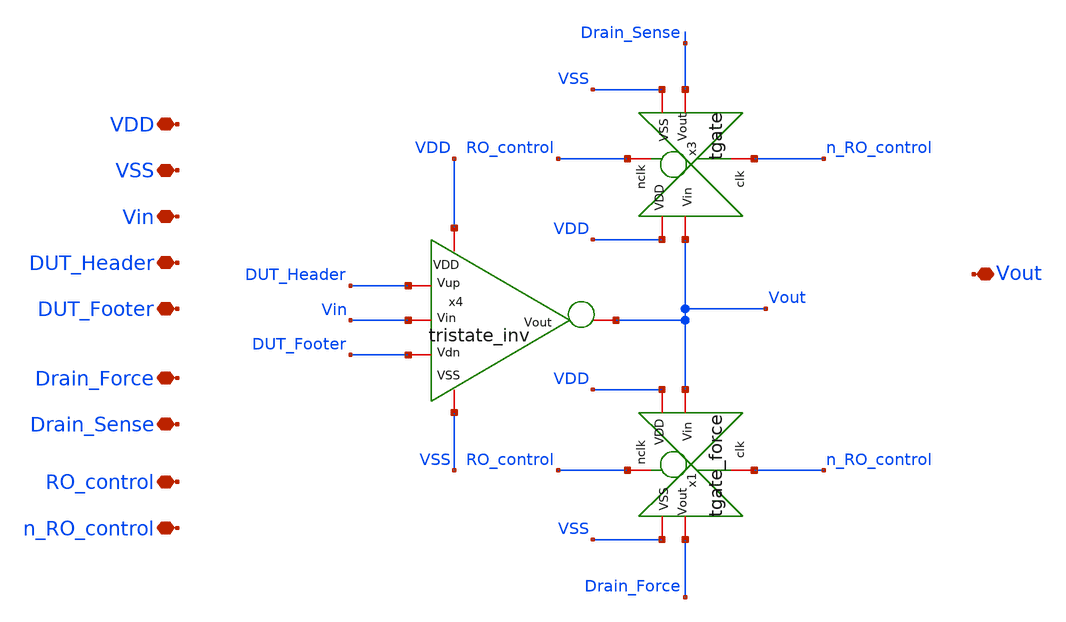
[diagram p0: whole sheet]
** sch_path: unic_cass_wrapper_user_project/ROs_reliability/rovcel1.sch
**.subckt rovcel1 VDD VSS Vin DUT_Header DUT_Footer Drain_Force Vout Drain_Sense RO_control
*+ n_RO_control
*.iopin VDD
*.iopin VSS
*.iopin Vin
*.iopin DUT_Header
*.iopin DUT_Footer
*.iopin Drain_Force
*.iopin Vout
*.iopin Drain_Sense
*.iopin RO_control
*.iopin n_RO_control
x4 VDD VSS Vin DUT_Header DUT_Footer Vout tristate_inv
x1 RO_control VDD Vout Drain_Force VSS n_RO_control tgate_force
x3 RO_control VDD Vout Drain_Sense VSS n_RO_control tgate
**.ends

* expanding   symbol:  tristate_inv.sym # of pins=6
** sym_path: tristate_inv.sym
** sch_path: tristate_inv.sch
.subckt tristate_inv VDD VSS Vin Vup Vdn Vout
*.iopin VDD
*.iopin VSS
*.iopin Vin
*.iopin Vout
*.iopin Vup
*.iopin Vdn
XM5 Vout Vin net1 VDD sg13_lv_pmos w=3.4u l=0.45u ng=1 m=4 mm_ok=1
XM2 net2 Vin Vout VSS sg13_lv_nmos w=1.3u l=0.45u ng=1 m=4 mm_ok=1
XM1 net1 Vup VDD VDD sg13_lv_pmos w=3.4u l=0.45u ng=1 m=12 mm_ok=1
XM3 VSS Vdn net2 VSS sg13_lv_nmos w=1.3u l=0.45u ng=1 m=12 mm_ok=1
.ends


* expanding   symbol:  tgate_force.sym # of pins=6
** sym_path: tgate_force.sym
** sch_path: tgate_force.sch
.subckt tgate_force nclk VDD Vin Vout VSS clk
*.iopin nclk
*.iopin clk
*.iopin VDD
*.iopin VSS
*.iopin Vout
*.iopin Vin
XM3 Vout nclk Vin VDD sg13_lv_pmos w=3.4u l=0.45u ng=1 m=4 mm_ok=1
XM4 Vout clk Vin VSS sg13_lv_nmos w=1.3u l=0.45u ng=1 m=4 mm_ok=1
.ends


* expanding   symbol:  tgate.sym # of pins=6
** sym_path: tgate.sym
** sch_path: tgate.sch
.subckt tgate nclk VDD Vin Vout VSS clk
*.iopin nclk
*.iopin clk
*.iopin VDD
*.iopin VSS
*.iopin Vout
*.iopin Vin
XM3 Vout nclk Vin VDD sg13_lv_pmos w=3.4u l=0.45u ng=1 m=1 mm_ok=1
XM1 Vout clk Vin VSS sg13_lv_nmos w=1.3u l=0.45u ng=1 m=1 mm_ok=1
.ends

.end
